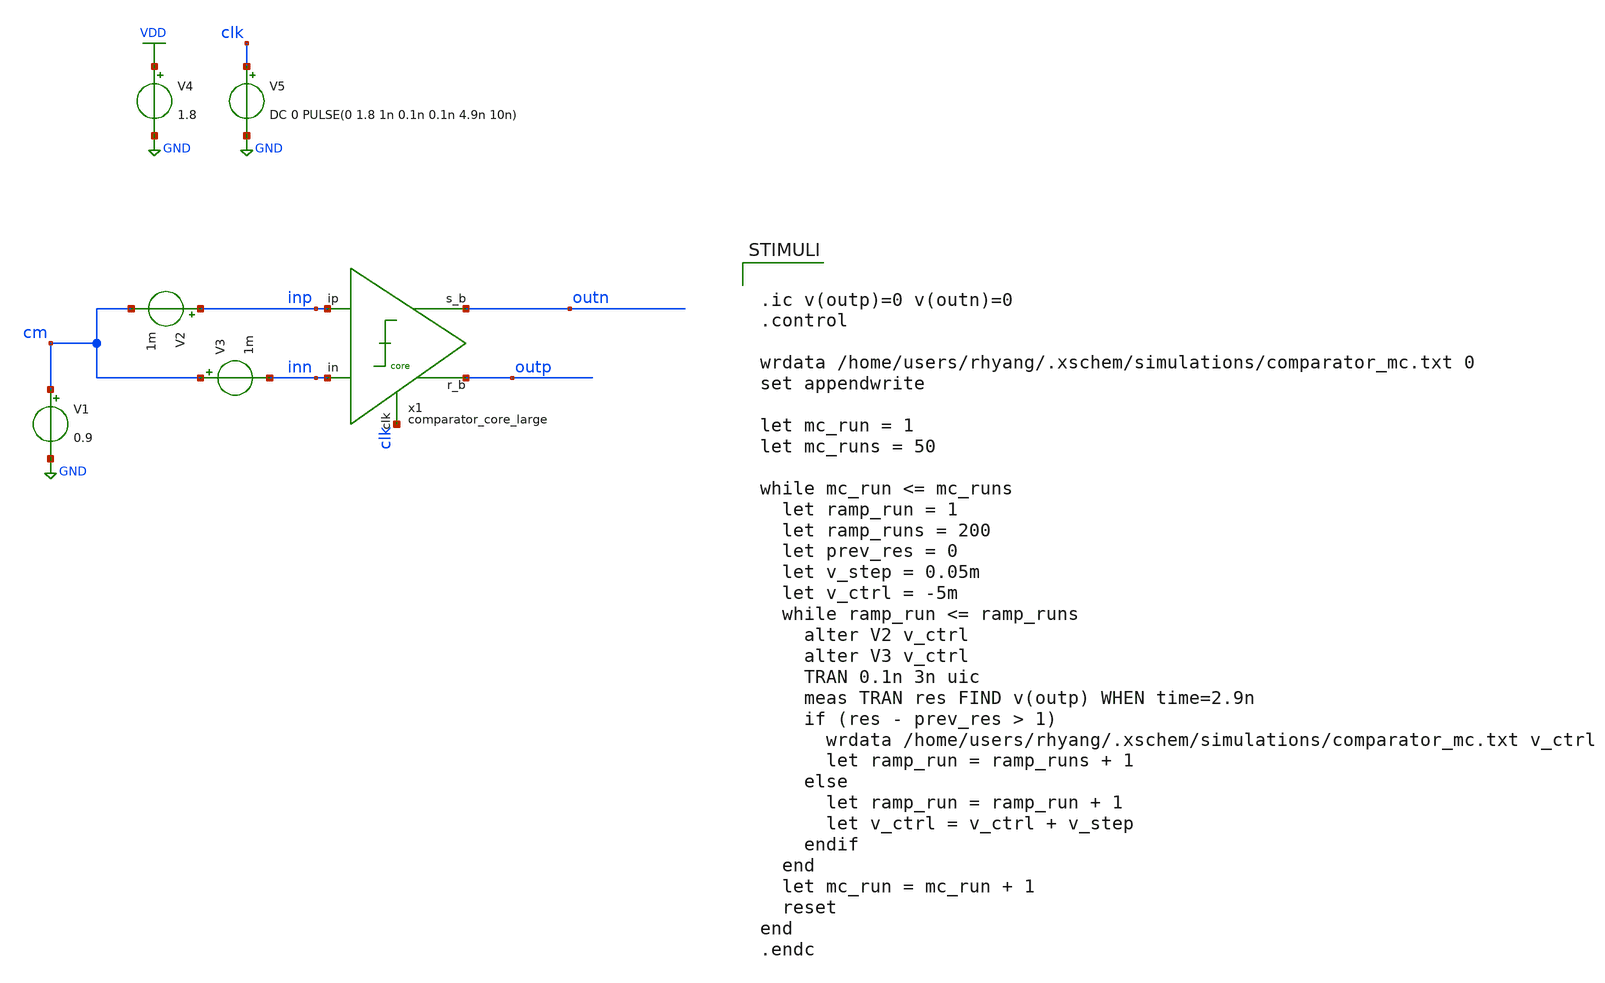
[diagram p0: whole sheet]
** sch_path: verification/schematic/comparator_tb_mcmm.sch
**.subckt comparator_tb_mcmm
V1 cm GND 0.9
V4 VDD GND 1.8
V5 clk GND DC 0 PULSE(0 1.8 1n 0.1n 0.1n 4.9n 10n)
V2 inp cm 1m
V3 cm inn 1m
x1 inp inn outn clk outp VDD GND comparator_core_large
**** begin user architecture code

** opencircuitdesign pdks install
.lib /farmshare/home/classes/ee/372/PDKs/open_pdks_1.0.310/sky130/sky130A/libs.tech/ngspice/sky130.lib.spice tt_mm



.ic v(outp)=0 v(outn)=0
.control

wrdata /home/users/rhyang/.xschem/simulations/comparator_mc.txt 0
set appendwrite

let mc_run = 1
let mc_runs = 50

while mc_run <= mc_runs
  let ramp_run = 1
  let ramp_runs = 200
  let prev_res = 0
  let v_step = 0.05m
  let v_ctrl = -5m
  while ramp_run <= ramp_runs
    alter V2 v_ctrl
    alter V3 v_ctrl
    TRAN 0.1n 3n uic
    meas TRAN res FIND v(outp) WHEN time=2.9n
    if (res - prev_res > 1)
      wrdata /home/users/rhyang/.xschem/simulations/comparator_mc.txt v_ctrl
      let ramp_run = ramp_runs + 1
    else
      let ramp_run = ramp_run + 1
      let v_ctrl = v_ctrl + v_step
    endif
  end
  let mc_run = mc_run + 1
  reset
end
.endc



**** end user architecture code
**.ends
.GLOBAL GND
.GLOBAL VDD
.end
